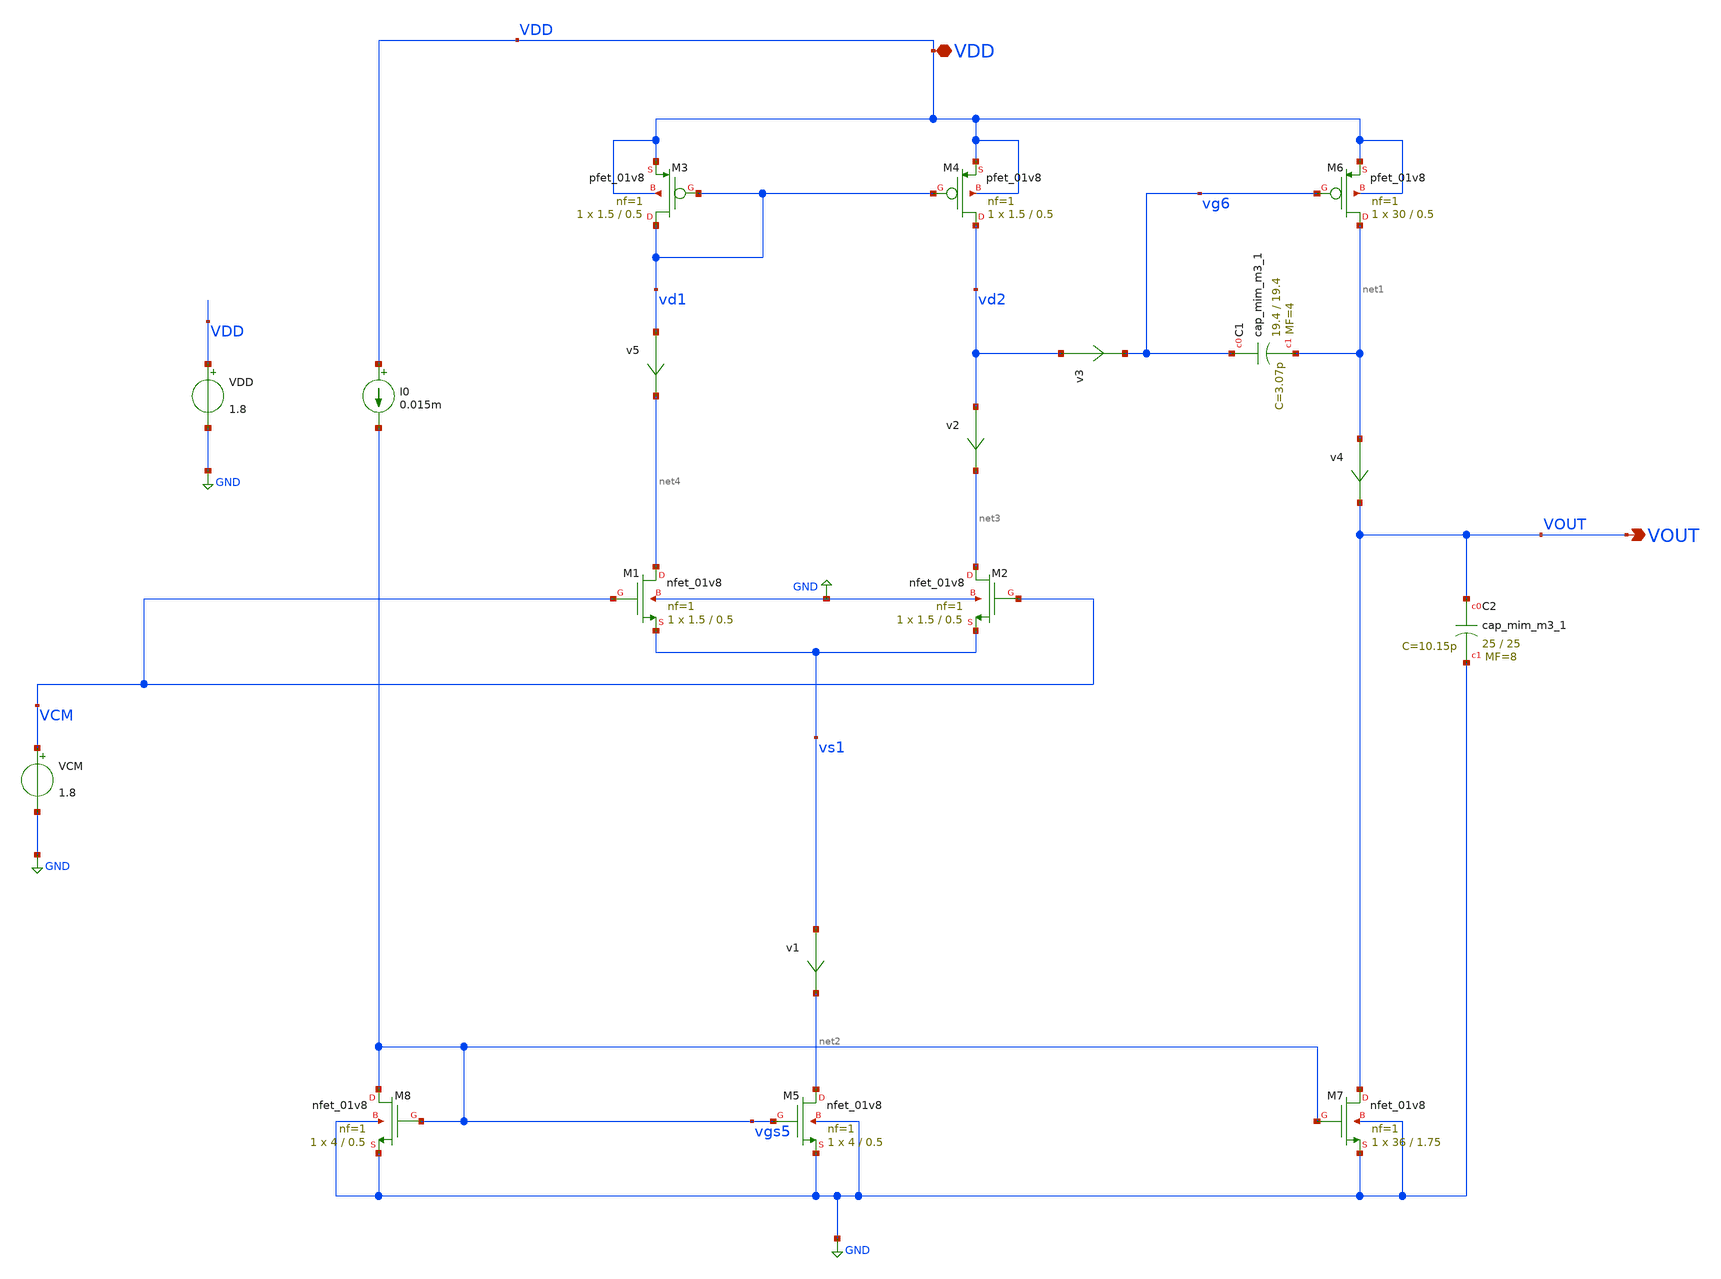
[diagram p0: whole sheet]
** sch_path: xschem/tso2.sch
**.subckt tso2 VOUT VDD
*.opin VOUT
*.iopin VDD
XM1 net4 VCM vs1 GND sky130_fd_pr__nfet_01v8 L=0.5 W=1.5 nf=1 ad='int((nf+1)/2) * W/nf * 0.29' as='int((nf+2)/2) * W/nf * 0.29'
+ pd='2*int((nf+1)/2) * (W/nf + 0.29)' ps='2*int((nf+2)/2) * (W/nf + 0.29)' nrd='0.29 / W' nrs='0.29 / W'
+ sa=0 sb=0 sd=0 mult=1 m=1
XM2 net3 VCM vs1 GND sky130_fd_pr__nfet_01v8 L=0.5 W=1.5 nf=1 ad='int((nf+1)/2) * W/nf * 0.29' as='int((nf+2)/2) * W/nf * 0.29'
+ pd='2*int((nf+1)/2) * (W/nf + 0.29)' ps='2*int((nf+2)/2) * (W/nf + 0.29)' nrd='0.29 / W' nrs='0.29 / W'
+ sa=0 sb=0 sd=0 mult=1 m=1
XM3 vd1 vd1 VDD VDD sky130_fd_pr__pfet_01v8 L=0.5 W=1.5 nf=1 ad='int((nf+1)/2) * W/nf * 0.29' as='int((nf+2)/2) * W/nf * 0.29'
+ pd='2*int((nf+1)/2) * (W/nf + 0.29)' ps='2*int((nf+2)/2) * (W/nf + 0.29)' nrd='0.29 / W' nrs='0.29 / W'
+ sa=0 sb=0 sd=0 mult=1 m=1
XM4 vd2 vd1 VDD VDD sky130_fd_pr__pfet_01v8 L=0.5 W=1.5 nf=1 ad='int((nf+1)/2) * W/nf * 0.29' as='int((nf+2)/2) * W/nf * 0.29'
+ pd='2*int((nf+1)/2) * (W/nf + 0.29)' ps='2*int((nf+2)/2) * (W/nf + 0.29)' nrd='0.29 / W' nrs='0.29 / W'
+ sa=0 sb=0 sd=0 mult=1 m=1
XM5 net2 vgs5 GND GND sky130_fd_pr__nfet_01v8 L=0.5 W=4 nf=1 ad='int((nf+1)/2) * W/nf * 0.29' as='int((nf+2)/2) * W/nf * 0.29'
+ pd='2*int((nf+1)/2) * (W/nf + 0.29)' ps='2*int((nf+2)/2) * (W/nf + 0.29)' nrd='0.29 / W' nrs='0.29 / W'
+ sa=0 sb=0 sd=0 mult=1 m=1
XM6 net1 vg6 VDD VDD sky130_fd_pr__pfet_01v8 L=0.5 W=30 nf=1 ad='int((nf+1)/2) * W/nf * 0.29' as='int((nf+2)/2) * W/nf * 0.29'
+ pd='2*int((nf+1)/2) * (W/nf + 0.29)' ps='2*int((nf+2)/2) * (W/nf + 0.29)' nrd='0.29 / W' nrs='0.29 / W'
+ sa=0 sb=0 sd=0 mult=1 m=1
XM7 VOUT vgs5 GND GND sky130_fd_pr__nfet_01v8 L=1.75 W=36 nf=1 ad='int((nf+1)/2) * W/nf * 0.29' as='int((nf+2)/2) * W/nf * 0.29'
+ pd='2*int((nf+1)/2) * (W/nf + 0.29)' ps='2*int((nf+2)/2) * (W/nf + 0.29)' nrd='0.29 / W' nrs='0.29 / W'
+ sa=0 sb=0 sd=0 mult=1 m=1
XM8 vgs5 vgs5 GND GND sky130_fd_pr__nfet_01v8 L=0.5 W=4 nf=1 ad='int((nf+1)/2) * W/nf * 0.29' as='int((nf+2)/2) * W/nf * 0.29'
+ pd='2*int((nf+1)/2) * (W/nf + 0.29)' ps='2*int((nf+2)/2) * (W/nf + 0.29)' nrd='0.29 / W' nrs='0.29 / W'
+ sa=0 sb=0 sd=0 mult=1 m=1
XC1 vg6 net1 sky130_fd_pr__cap_mim_m3_1 W=19.4 L=19.4 MF=4 m=4
XC2 VOUT GND sky130_fd_pr__cap_mim_m3_1 W=25 L=25 MF=8 m=8
I0 VDD vgs5 0.015m
v5 vd1 net4 0
.save i(v5)
v1 vs1 net2 0
.save i(v1)
VDD VDD GND 1.8
VCM VCM GND 1.8
v2 vd2 net3 0
.save i(v2)
v3 vd2 vg6 0
.save i(v3)
v4 net1 VOUT 0
.save i(v4)
**** begin user architecture code

** opencircuitdesign pdks install
.lib $::SKYWATER_MODELS/sky130.lib.spice tt




.options acct list
.temp 25
.save all

.save @m.xm1.msky130_fd_pr__nfet_01v8[vth]
.save @m.xm1.msky130_fd_pr__nfet_01v8[gm]

.save @m.xm2.msky130_fd_pr__nfet_01v8[vth]
.save @m.xm2.msky130_fd_pr__nfet_01v8[gm]

.save @m.xm3.msky130_fd_pr__pfet_01v8[vth]
.save @m.xm3.msky130_fd_pr__pfet_01v8[gm]

.save @m.xm4.msky130_fd_pr__pfet_01v8[vth]
.save @m.xm4.msky130_fd_pr__pfet_01v8[gm]

.save @m.xm5.msky130_fd_pr__nfet_01v8[vth]
.save @m.xm5.msky130_fd_pr__nfet_01v8[gm]

.save @m.xm6.msky130_fd_pr__pfet_01v8[vth]
.save @m.xm6.msky130_fd_pr__pfet_01v8[gm]

.save @m.xm7.msky130_fd_pr__nfet_01v8[vth]
.save @m.xm7.msky130_fd_pr__nfet_01v8[gm]

.save @m.xm8.msky130_fd_pr__nfet_01v8[vth]
.save @m.xm8.msky130_fd_pr__nfet_01v8[gm]

.control
op
dc VCM 0 1.8 0.3

remzerovec
write tso2.raw

.endc



**** end user architecture code
**.ends
.GLOBAL GND
.end
